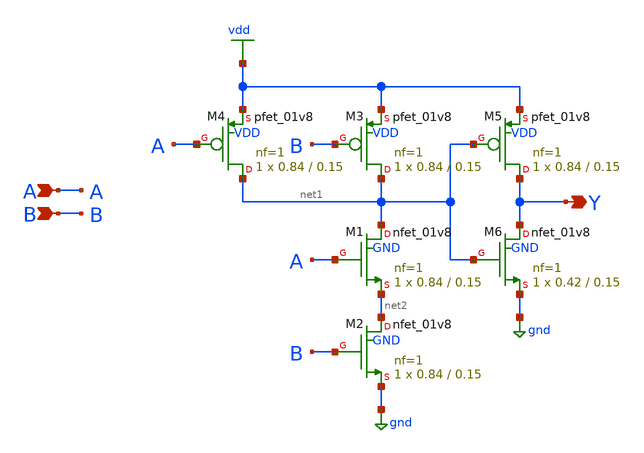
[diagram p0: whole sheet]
** sch_path: xschem/and2.sch
**.subckt and2 A B Y
*.ipin A
*.ipin B
*.opin Y
XM1 net1 A net2 GND sky130_fd_pr__nfet_01v8 L=0.15 W=0.84 nf=1 ad='int((nf+1)/2) * W/nf * 0.29' as='int((nf+2)/2) * W/nf * 0.29'
+ pd='2*int((nf+1)/2) * (W/nf + 0.29)' ps='2*int((nf+2)/2) * (W/nf + 0.29)' nrd='0.29 / W' nrs='0.29 / W'
+ sa=0 sb=0 sd=0 mult=1 m=1
XM2 net2 B gnd GND sky130_fd_pr__nfet_01v8 L=0.15 W=0.84 nf=1 ad='int((nf+1)/2) * W/nf * 0.29' as='int((nf+2)/2) * W/nf * 0.29'
+ pd='2*int((nf+1)/2) * (W/nf + 0.29)' ps='2*int((nf+2)/2) * (W/nf + 0.29)' nrd='0.29 / W' nrs='0.29 / W'
+ sa=0 sb=0 sd=0 mult=1 m=1
XM3 net1 B vdd VDD sky130_fd_pr__pfet_01v8 L=0.15 W=0.84 nf=1 ad='int((nf+1)/2) * W/nf * 0.29' as='int((nf+2)/2) * W/nf * 0.29'
+ pd='2*int((nf+1)/2) * (W/nf + 0.29)' ps='2*int((nf+2)/2) * (W/nf + 0.29)' nrd='0.29 / W' nrs='0.29 / W'
+ sa=0 sb=0 sd=0 mult=1 m=1
XM4 net1 A vdd VDD sky130_fd_pr__pfet_01v8 L=0.15 W=0.84 nf=1 ad='int((nf+1)/2) * W/nf * 0.29' as='int((nf+2)/2) * W/nf * 0.29'
+ pd='2*int((nf+1)/2) * (W/nf + 0.29)' ps='2*int((nf+2)/2) * (W/nf + 0.29)' nrd='0.29 / W' nrs='0.29 / W'
+ sa=0 sb=0 sd=0 mult=1 m=1
XM5 Y net1 vdd VDD sky130_fd_pr__pfet_01v8 L=0.15 W=0.84 nf=1 ad='int((nf+1)/2) * W/nf * 0.29' as='int((nf+2)/2) * W/nf * 0.29'
+ pd='2*int((nf+1)/2) * (W/nf + 0.29)' ps='2*int((nf+2)/2) * (W/nf + 0.29)' nrd='0.29 / W' nrs='0.29 / W'
+ sa=0 sb=0 sd=0 mult=1 m=1
XM6 Y net1 gnd GND sky130_fd_pr__nfet_01v8 L=0.15 W=0.42 nf=1 ad='int((nf+1)/2) * W/nf * 0.29' as='int((nf+2)/2) * W/nf * 0.29'
+ pd='2*int((nf+1)/2) * (W/nf + 0.29)' ps='2*int((nf+2)/2) * (W/nf + 0.29)' nrd='0.29 / W' nrs='0.29 / W'
+ sa=0 sb=0 sd=0 mult=1 m=1
**.ends
.GLOBAL gnd
.GLOBAL vdd
.end
